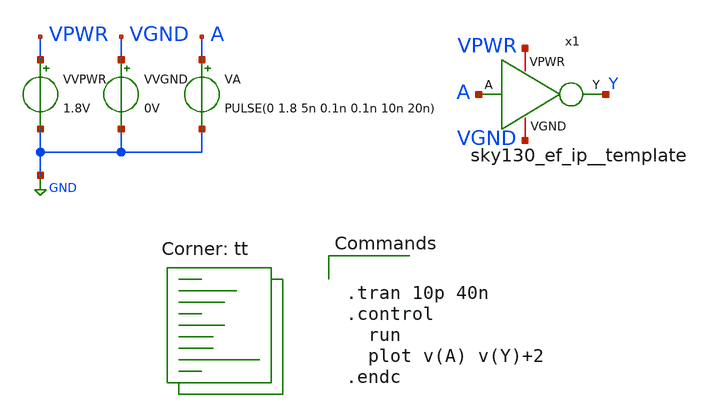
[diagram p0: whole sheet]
** sch_path: xschem/sky130_ef_ip__template_tb.sch
**.subckt sky130_ef_ip__template_tb
x1 VPWR A Y VGND sky130_ef_ip__template
VVPWR VPWR GND 1.8V
VVGND VGND GND 0V
VA A GND PULSE(0 1.8 5n 0.1n 0.1n 10n 20n)
**** begin user architecture code


.tran 10p 40n
.control
  run
  plot v(A) v(Y)+2
.endc


.lib $::SKYWATER_MODELS/sky130.lib.spice tt
**** end user architecture code
**.ends

* expanding   symbol:  sky130_ef_ip__template/sky130_ef_ip__template.sym # of pins=4
** sym_path: xschem/sky130_ef_ip__template.sym
** sch_path: xschem/sky130_ef_ip__template.sch
.subckt sky130_ef_ip__template VPWR A Y VGND
*.iopin VPWR
*.iopin VGND
*.ipin A
*.opin Y
XM1 Y A VGND VGND sky130_fd_pr__nfet_01v8 L=0.15 W=1 nf=1 ad='int((nf+1)/2) * W/nf * 0.29' as='int((nf+2)/2) * W/nf * 0.29'
+ pd='2*int((nf+1)/2) * (W/nf + 0.29)' ps='2*int((nf+2)/2) * (W/nf + 0.29)' nrd='0.29 / W' nrs='0.29 / W'
+ sa=0 sb=0 sd=0 mult=1 m=1
XM2 Y A VPWR VPWR sky130_fd_pr__pfet_01v8 L=0.15 W=1 nf=1 ad='int((nf+1)/2) * W/nf * 0.29' as='int((nf+2)/2) * W/nf * 0.29'
+ pd='2*int((nf+1)/2) * (W/nf + 0.29)' ps='2*int((nf+2)/2) * (W/nf + 0.29)' nrd='0.29 / W' nrs='0.29 / W'
+ sa=0 sb=0 sd=0 mult=1 m=1
.ends

.GLOBAL GND
.end
